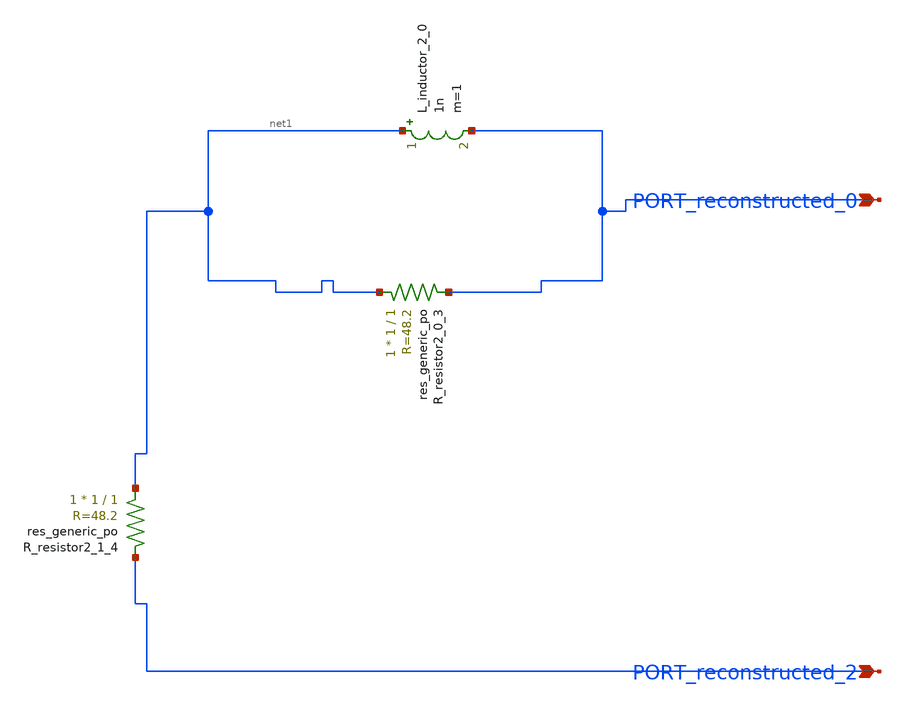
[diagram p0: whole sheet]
** sch_path: schematics/AMSNet/375.sch
**.subckt 375 PORT_reconstructed_0 PORT_reconstructed_2
*.ipin PORT_reconstructed_0
*.ipin PORT_reconstructed_2
L_inductor_2_0 net1 PORT_reconstructed_0 1n m=1
XR_resistor2_0_3 net1 PORT_reconstructed_0 sky130_fd_pr__res_generic_po W=1 L=1 m=1
XR_resistor2_1_4 net1 PORT_reconstructed_2 sky130_fd_pr__res_generic_po W=1 L=1 m=1
**.ends
.end
